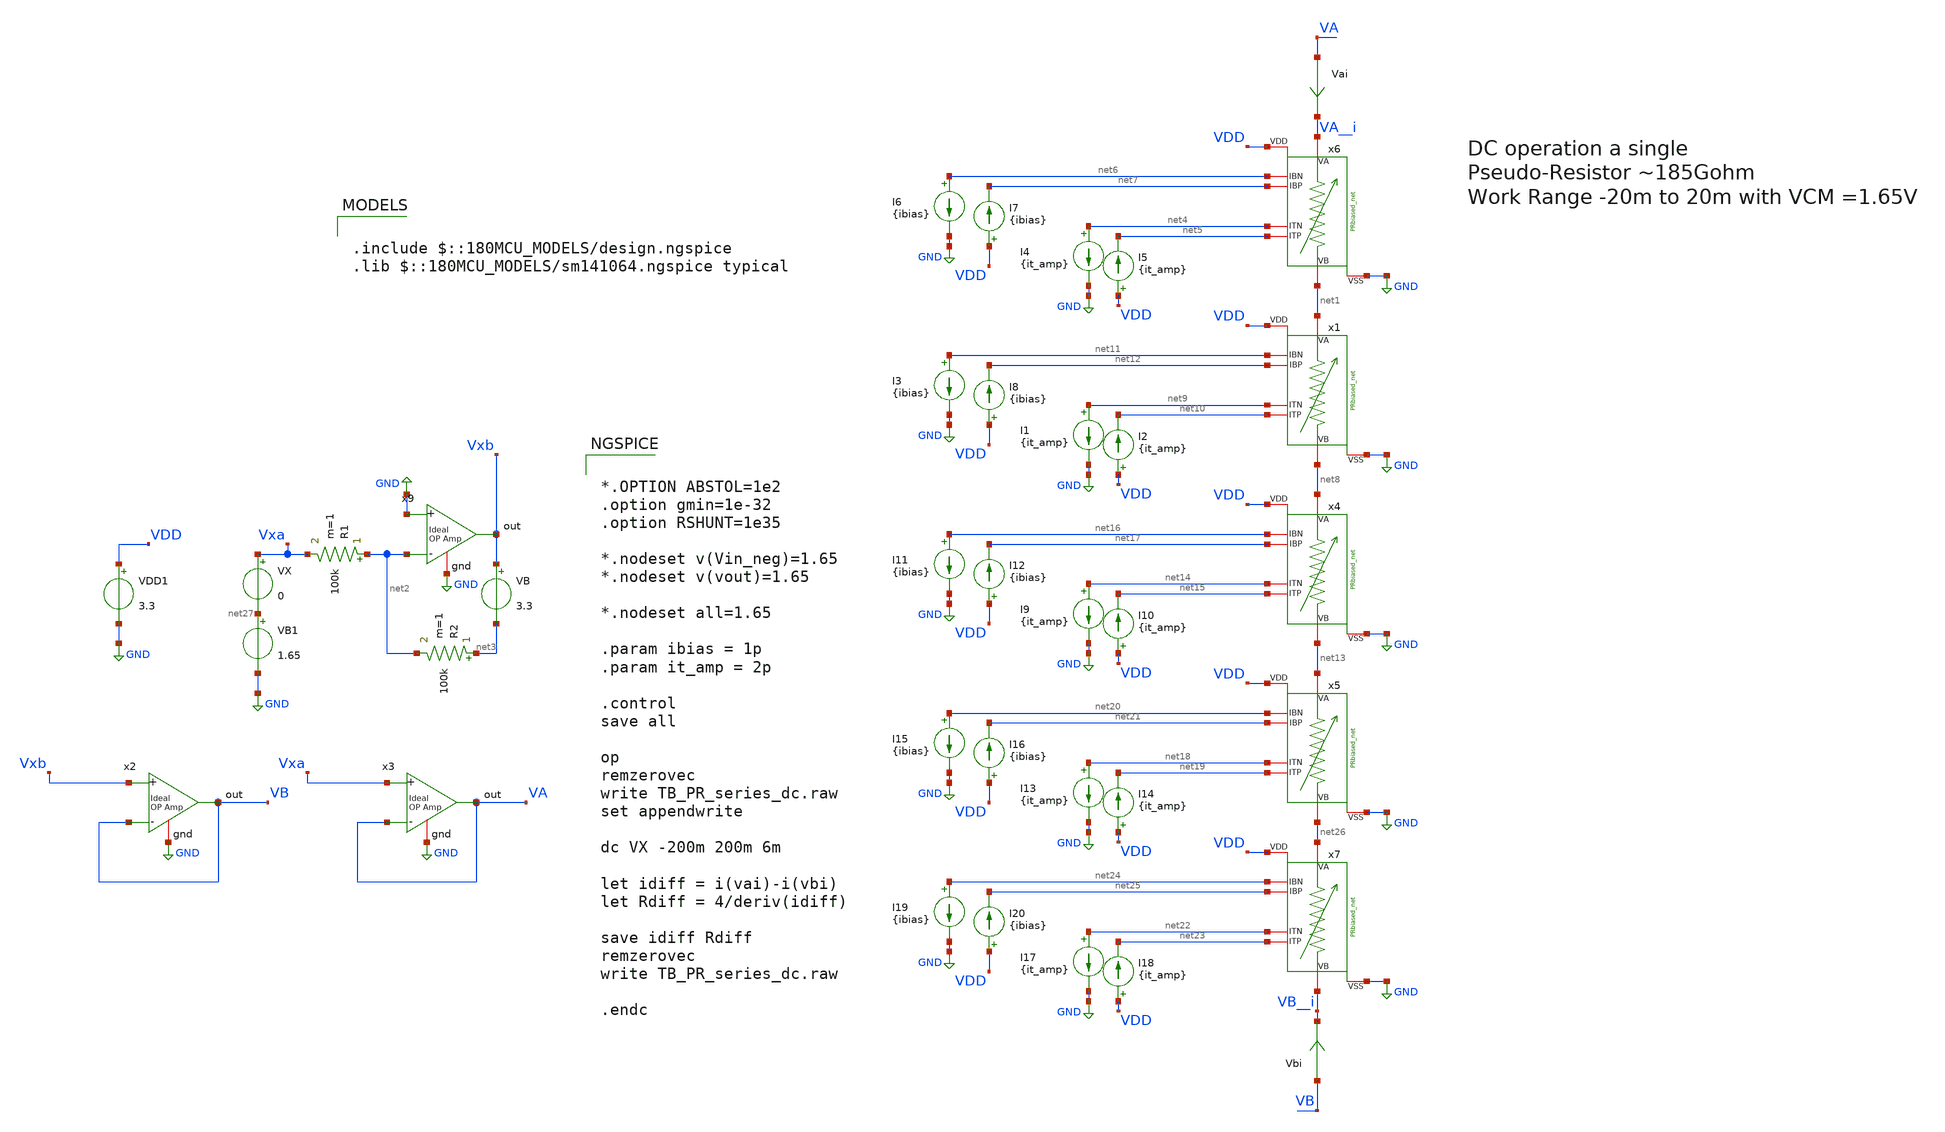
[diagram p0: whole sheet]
** sch_path: TIA/PseudoResistor/TB_PR_series_dc.sch
**.subckt TB_PR_series_dc
VDD1 VDD GND 3.3
VX Vxa net27 0
VB Vxb net3 3.3
R1 net2 Vxa 100k m=1
R2 net3 net2 100k m=1
VB1 net27 GND 1.65
x2 VB Vxb VB GND ampOp_ideal
x3 VA Vxa VA GND ampOp_ideal
x9 Vxb GND net2 GND ampOp_ideal
Vai VA VA__i 0
.save i(vai)
x6 VA__i net1 net6 net7 net4 net5 VDD GND PRbiased_net
I4 net4 GND {it_amp}
I5 VDD net5 {it_amp}
I6 net6 GND {ibias}
I7 VDD net7 {ibias}
x1 net1 net8 net11 net12 net9 net10 VDD GND PRbiased_net
I1 net9 GND {it_amp}
I2 VDD net10 {it_amp}
I3 net11 GND {ibias}
I8 VDD net12 {ibias}
x4 net8 net13 net16 net17 net14 net15 VDD GND PRbiased_net
I9 net14 GND {it_amp}
I10 VDD net15 {it_amp}
I11 net16 GND {ibias}
I12 VDD net17 {ibias}
x5 net13 net26 net20 net21 net18 net19 VDD GND PRbiased_net
I13 net18 GND {it_amp}
I14 VDD net19 {it_amp}
I15 net20 GND {ibias}
I16 VDD net21 {ibias}
x7 net26 VB__i net24 net25 net22 net23 VDD GND PRbiased_net
I17 net22 GND {it_amp}
I18 VDD net23 {it_amp}
I19 net24 GND {ibias}
I20 VDD net25 {ibias}
Vbi VB VB__i 0
.save i(vbi)
**** begin user architecture code

.include $::180MCU_MODELS/design.ngspice
.lib $::180MCU_MODELS/sm141064.ngspice typical



*.OPTION ABSTOL=1e2
.option gmin=1e-32
.option RSHUNT=1e35

*.nodeset v(Vin_neg)=1.65
*.nodeset v(vout)=1.65

*.nodeset all=1.65

.param ibias = 1p
.param it_amp = 2p

.control
save all

op
remzerovec
write TB_PR_series_dc.raw
set appendwrite

dc VX -200m 200m 6m

let idiff = i(vai)-i(vbi)
let Rdiff = 4/deriv(idiff)

save idiff Rdiff
remzerovec
write TB_PR_series_dc.raw

.endc


**** end user architecture code
**.ends
.GLOBAL GND
.end
